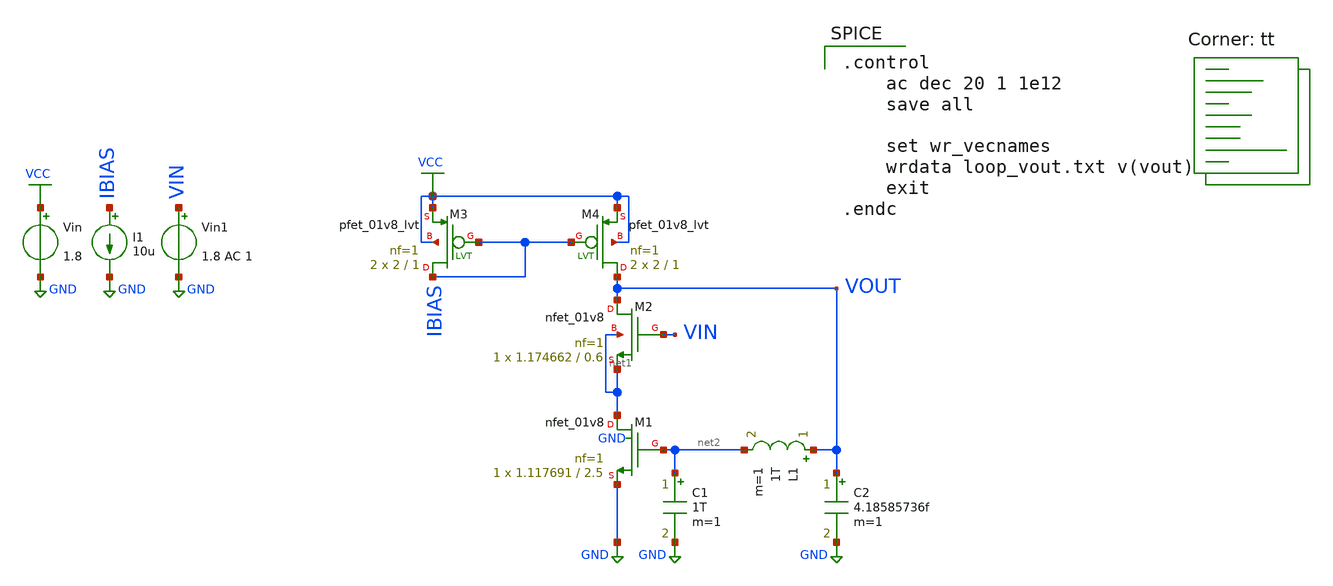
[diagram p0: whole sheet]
** sch_path: xschem/fvf_tb_loop.sch
**.subckt fvf_tb_loop
Vin VCC GND 1.8
Vin1 VIN GND 1.8 AC 1
I1 IBIAS GND 10u
L1 VOUT net2 1T m=1
C1 net2 GND 1T m=1
C2 VOUT GND 4.18585736f m=1
XM3 IBIAS IBIAS VCC VCC sky130_fd_pr__pfet_01v8_lvt L=1 W=2 nf=1 ad='int((nf+1)/2) * W/nf * 0.29' as='int((nf+2)/2) * W/nf * 0.29'
+ pd='2*int((nf+1)/2) * (W/nf + 0.29)' ps='2*int((nf+2)/2) * (W/nf + 0.29)' nrd='0.29 / W' nrs='0.29 / W'
+ sa=0 sb=0 sd=0 mult=2 m=2
XM4 VOUT IBIAS VCC VCC sky130_fd_pr__pfet_01v8_lvt L=1 W=2 nf=1 ad='int((nf+1)/2) * W/nf * 0.29' as='int((nf+2)/2) * W/nf * 0.29'
+ pd='2*int((nf+1)/2) * (W/nf + 0.29)' ps='2*int((nf+2)/2) * (W/nf + 0.29)' nrd='0.29 / W' nrs='0.29 / W'
+ sa=0 sb=0 sd=0 mult=2 m=2
XM1 net1 net2 GND GND sky130_fd_pr__nfet_01v8 L=2.5 W=1.117691 nf=1 ad='int((nf+1)/2) * W/nf * 0.29'
+ as='int((nf+2)/2) * W/nf * 0.29' pd='2*int((nf+1)/2) * (W/nf + 0.29)' ps='2*int((nf+2)/2) * (W/nf + 0.29)'
+ nrd='0.29 / W' nrs='0.29 / W' sa=0 sb=0 sd=0 mult=1 m=1
XM2 VOUT VIN net1 net1 sky130_fd_pr__nfet_01v8 L=0.6 W=1.174662 nf=1 ad='int((nf+1)/2) * W/nf * 0.29'
+ as='int((nf+2)/2) * W/nf * 0.29' pd='2*int((nf+1)/2) * (W/nf + 0.29)' ps='2*int((nf+2)/2) * (W/nf + 0.29)'
+ nrd='0.29 / W' nrs='0.29 / W' sa=0 sb=0 sd=0 mult=1 m=1
**** begin user architecture code
.lib $::SKYWATER_MODELS/sky130.lib.spice tt

.control
    ac dec 20 1 1e12
    save all

    set wr_vecnames
    wrdata loop_vout.txt v(vout)
    exit
.endc

**** end user architecture code
**.ends
.GLOBAL VCC
.GLOBAL GND
.end
